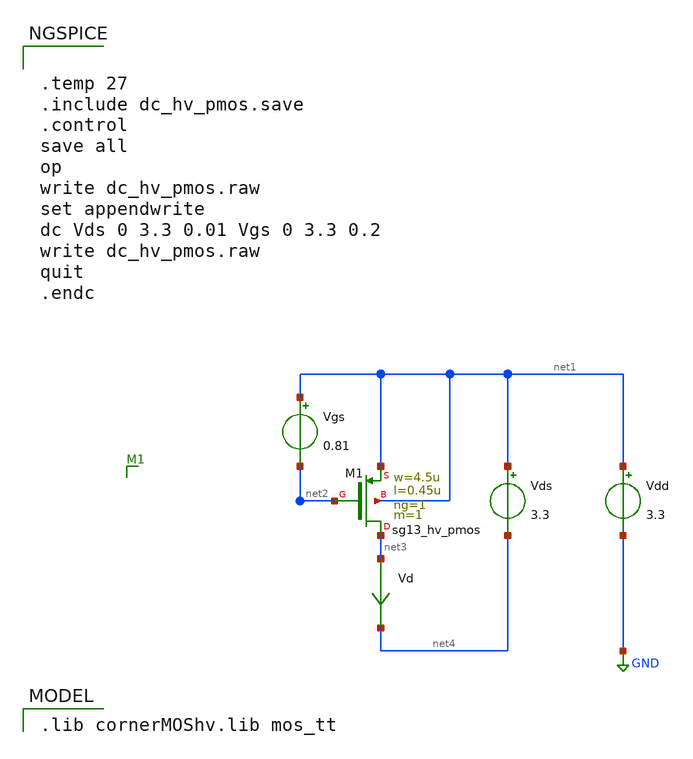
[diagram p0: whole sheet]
** sch_path: xschem/dc_hv_pmos.sch
* (c) 2023-2025 Harald Pretl, Apache-2.0 license
**.subckt dc_hv_pmos
Vgs net1 net2 0.81
Vds net1 net4 3.3
Vd net3 net4 0
.save i(vd)
Vdd net1 GND 3.3
XM1 net3 net2 net1 net1 sg13_hv_pmos w=4.5u l=0.45u ng=1 m=1 mm_ok=1
**** begin user architecture code
 .lib cornerMOShv.lib mos_tt



.temp 27
.include dc_hv_pmos.save
.control
save all
op
write dc_hv_pmos.raw
set appendwrite
dc Vds 0 3.3 0.01 Vgs 0 3.3 0.2
write dc_hv_pmos.raw
quit
.endc


**** end user architecture code
**.ends
.GLOBAL GND
.end
